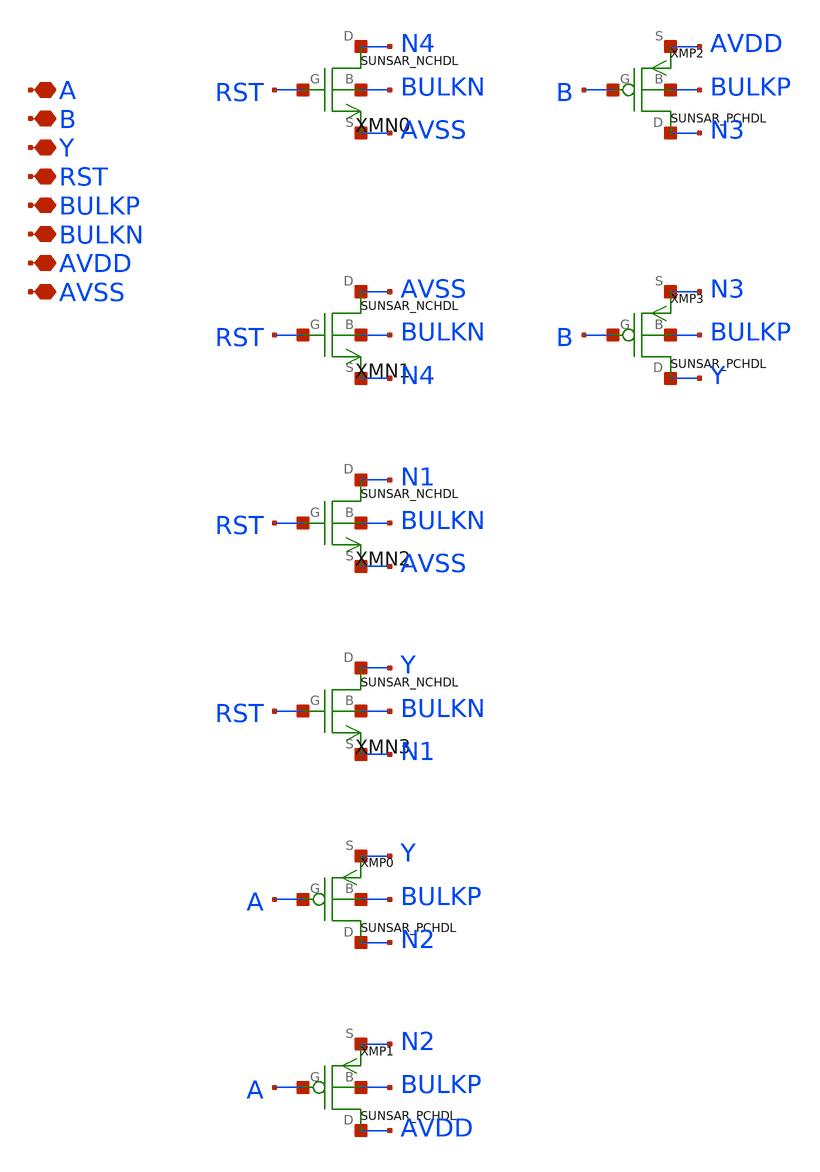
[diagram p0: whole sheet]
** sch_path: ip/sun_sar9b_sky130nm/design/SUN_SAR9B_SKY130NM/SUNSAR_SARCEX1_CV.sch
**.subckt SUNSAR_SARCEX1_CV A B Y RST BULKP BULKN AVDD AVSS
*.iopin A
*.iopin B
*.iopin Y
*.iopin RST
*.iopin BULKP
*.iopin BULKN
*.iopin AVDD
*.iopin AVSS
XMN0 N4 RST AVSS BULKN SUNSAR_NCHDL
XMN1 AVSS RST N4 BULKN SUNSAR_NCHDL
XMN2 N1 RST AVSS BULKN SUNSAR_NCHDL
XMN3 Y RST N1 BULKN SUNSAR_NCHDL
XMP0 N2 A Y BULKP SUNSAR_PCHDL
XMP1 AVDD A N2 BULKP SUNSAR_PCHDL
XMP2 N3 B AVDD BULKP SUNSAR_PCHDL
XMP3 Y B N3 BULKP SUNSAR_PCHDL
**.ends
.end
